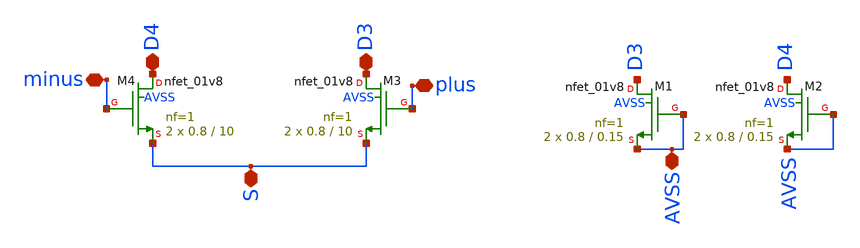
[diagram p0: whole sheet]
** sch_path: magic/differential_pair.sch
**.subckt differential_pair minus plus D3 D4 S AVSS
*.iopin minus
*.iopin plus
*.iopin D3
*.iopin D4
*.iopin S
*.iopin AVSS
XM3 D3 plus S AVSS sky130_fd_pr__nfet_01v8 L=10 W=0.8 nf=1 ad='int((nf+1)/2) * W/nf * 0.29' as='int((nf+2)/2) * W/nf * 0.29'
+ pd='2*int((nf+1)/2) * (W/nf + 0.29)' ps='2*int((nf+2)/2) * (W/nf + 0.29)' nrd='0.29 / W' nrs='0.29 / W'
+ sa=0 sb=0 sd=0 mult=2 m=2
XM4 D4 minus S AVSS sky130_fd_pr__nfet_01v8 L=10 W=0.8 nf=1 ad='int((nf+1)/2) * W/nf * 0.29' as='int((nf+2)/2) * W/nf * 0.29'
+ pd='2*int((nf+1)/2) * (W/nf + 0.29)' ps='2*int((nf+2)/2) * (W/nf + 0.29)' nrd='0.29 / W' nrs='0.29 / W'
+ sa=0 sb=0 sd=0 mult=2 m=2
XM1 D3 AVSS AVSS AVSS sky130_fd_pr__nfet_01v8 L=0.15 W=0.8 nf=1 ad='int((nf+1)/2) * W/nf * 0.29' as='int((nf+2)/2) * W/nf * 0.29'
+ pd='2*int((nf+1)/2) * (W/nf + 0.29)' ps='2*int((nf+2)/2) * (W/nf + 0.29)' nrd='0.29 / W' nrs='0.29 / W'
+ sa=0 sb=0 sd=0 mult=2 m=2
XM2 D4 AVSS AVSS AVSS sky130_fd_pr__nfet_01v8 L=0.15 W=0.8 nf=1 ad='int((nf+1)/2) * W/nf * 0.29' as='int((nf+2)/2) * W/nf * 0.29'
+ pd='2*int((nf+1)/2) * (W/nf + 0.29)' ps='2*int((nf+2)/2) * (W/nf + 0.29)' nrd='0.29 / W' nrs='0.29 / W'
+ sa=0 sb=0 sd=0 mult=2 m=2
**.ends
.end
